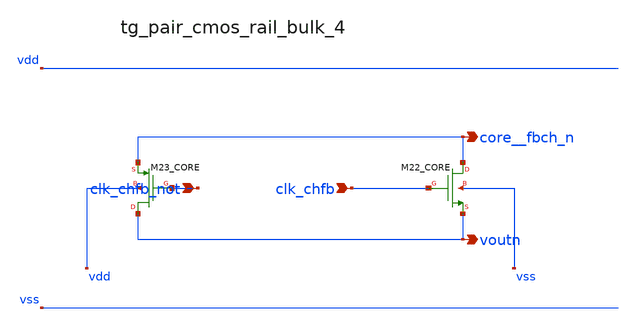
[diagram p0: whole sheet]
** sch_path: analog-db/raw/ia_006_fan_chopper_cmfb/hier/blocks/tg_pair_cmos_rail_bulk_4.sch
**.subckt tg_pair_cmos_rail_bulk_4 clk_chfb_not clk_chfb core__fbch_n voutn
*.ipin clk_chfb_not
*.ipin clk_chfb
*.opin core__fbch_n
*.opin voutn
XM22_CORE core__fbch_n clk_chfb voutn vss sg13_lv_nmos w=x_dut_xm22_core_w l=x_dut_xm22_core_l ng=1
+ m=x_dut_xm22_core_m
XM23_CORE voutn clk_chfb_not core__fbch_n vdd sg13_lv_pmos w=x_dut_xm23_core_w l=x_dut_xm23_core_l
+ ng=1 m=x_dut_xm23_core_m
**.ends
.end
